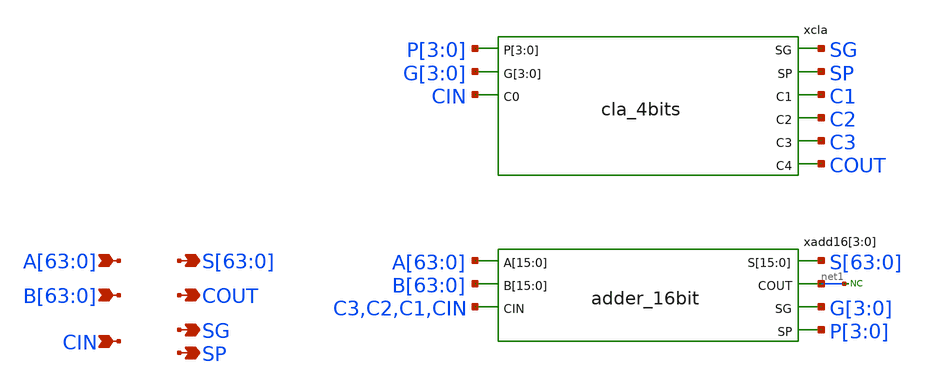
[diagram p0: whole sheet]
** sch_path: sky130A/xschem_libs/sky130_tests/adder_64bit/schematic/adder_64bit.sch
**.subckt adder_64bit
*+ A[63],A[62],A[61],A[60],A[59],A[58],A[57],A[56],A[55],A[54],A[53],A[52],A[51],A[50],A[49],A[48],A[47],A[46],A[45],A[44],A[43],A[42],A[41],A[40],A[39],A[38],A[37],A[36],A[35],A[34],A[33],A[32],A[31],A[30],A[29],A[28],A[27],A[26],A[25],A[24],A[23],A[22],A[21],A[20],A[19],A[18],A[17],A[16],A[15],A[14],A[13],A[12],A[11],A[10],A[9],A[8],A[7],A[6],A[5],A[4],A[3],A[2],A[1],A[0]
*+ B[63],B[62],B[61],B[60],B[59],B[58],B[57],B[56],B[55],B[54],B[53],B[52],B[51],B[50],B[49],B[48],B[47],B[46],B[45],B[44],B[43],B[42],B[41],B[40],B[39],B[38],B[37],B[36],B[35],B[34],B[33],B[32],B[31],B[30],B[29],B[28],B[27],B[26],B[25],B[24],B[23],B[22],B[21],B[20],B[19],B[18],B[17],B[16],B[15],B[14],B[13],B[12],B[11],B[10],B[9],B[8],B[7],B[6],B[5],B[4],B[3],B[2],B[1],B[0] CIN
*+ S[63],S[62],S[61],S[60],S[59],S[58],S[57],S[56],S[55],S[54],S[53],S[52],S[51],S[50],S[49],S[48],S[47],S[46],S[45],S[44],S[43],S[42],S[41],S[40],S[39],S[38],S[37],S[36],S[35],S[34],S[33],S[32],S[31],S[30],S[29],S[28],S[27],S[26],S[25],S[24],S[23],S[22],S[21],S[20],S[19],S[18],S[17],S[16],S[15],S[14],S[13],S[12],S[11],S[10],S[9],S[8],S[7],S[6],S[5],S[4],S[3],S[2],S[1],S[0] SP SG COUT
*.ipin
*+ A[63],A[62],A[61],A[60],A[59],A[58],A[57],A[56],A[55],A[54],A[53],A[52],A[51],A[50],A[49],A[48],A[47],A[46],A[45],A[44],A[43],A[42],A[41],A[40],A[39],A[38],A[37],A[36],A[35],A[34],A[33],A[32],A[31],A[30],A[29],A[28],A[27],A[26],A[25],A[24],A[23],A[22],A[21],A[20],A[19],A[18],A[17],A[16],A[15],A[14],A[13],A[12],A[11],A[10],A[9],A[8],A[7],A[6],A[5],A[4],A[3],A[2],A[1],A[0]
*.ipin
*+ B[63],B[62],B[61],B[60],B[59],B[58],B[57],B[56],B[55],B[54],B[53],B[52],B[51],B[50],B[49],B[48],B[47],B[46],B[45],B[44],B[43],B[42],B[41],B[40],B[39],B[38],B[37],B[36],B[35],B[34],B[33],B[32],B[31],B[30],B[29],B[28],B[27],B[26],B[25],B[24],B[23],B[22],B[21],B[20],B[19],B[18],B[17],B[16],B[15],B[14],B[13],B[12],B[11],B[10],B[9],B[8],B[7],B[6],B[5],B[4],B[3],B[2],B[1],B[0]
*.ipin CIN
*.opin
*+ S[63],S[62],S[61],S[60],S[59],S[58],S[57],S[56],S[55],S[54],S[53],S[52],S[51],S[50],S[49],S[48],S[47],S[46],S[45],S[44],S[43],S[42],S[41],S[40],S[39],S[38],S[37],S[36],S[35],S[34],S[33],S[32],S[31],S[30],S[29],S[28],S[27],S[26],S[25],S[24],S[23],S[22],S[21],S[20],S[19],S[18],S[17],S[16],S[15],S[14],S[13],S[12],S[11],S[10],S[9],S[8],S[7],S[6],S[5],S[4],S[3],S[2],S[1],S[0]
*.opin SP
*.opin SG
*.opin COUT
xadd16[3] A[63] A[62] A[61] A[60] A[59] A[58] A[57] A[56] A[55] A[54] A[53] A[52] A[51] A[50] A[49]
+ A[48] S[63] S[62] S[61] S[60] S[59] S[58] S[57] S[56] S[55] S[54] S[53] S[52] S[51] S[50] S[49] S[48]
+ B[63] B[62] B[61] B[60] B[59] B[58] B[57] B[56] B[55] B[54] B[53] B[52] B[51] B[50] B[49] B[48] net1 G[3]
+ C3 P[3] adder_16bit
xadd16[2] A[47] A[46] A[45] A[44] A[43] A[42] A[41] A[40] A[39] A[38] A[37] A[36] A[35] A[34] A[33]
+ A[32] S[47] S[46] S[45] S[44] S[43] S[42] S[41] S[40] S[39] S[38] S[37] S[36] S[35] S[34] S[33] S[32]
+ B[47] B[46] B[45] B[44] B[43] B[42] B[41] B[40] B[39] B[38] B[37] B[36] B[35] B[34] B[33] B[32] net1 G[2]
+ C2 P[2] adder_16bit
xadd16[1] A[31] A[30] A[29] A[28] A[27] A[26] A[25] A[24] A[23] A[22] A[21] A[20] A[19] A[18] A[17]
+ A[16] S[31] S[30] S[29] S[28] S[27] S[26] S[25] S[24] S[23] S[22] S[21] S[20] S[19] S[18] S[17] S[16]
+ B[31] B[30] B[29] B[28] B[27] B[26] B[25] B[24] B[23] B[22] B[21] B[20] B[19] B[18] B[17] B[16] net1 G[1]
+ C1 P[1] adder_16bit
xadd16[0] A[15] A[14] A[13] A[12] A[11] A[10] A[9] A[8] A[7] A[6] A[5] A[4] A[3] A[2] A[1] A[0]
+ S[15] S[14] S[13] S[12] S[11] S[10] S[9] S[8] S[7] S[6] S[5] S[4] S[3] S[2] S[1] S[0] B[15] B[14] B[13]
+ B[12] B[11] B[10] B[9] B[8] B[7] B[6] B[5] B[4] B[3] B[2] B[1] B[0] net1 G[0] CIN P[0] adder_16bit
xcla SG SP C1 P[3] P[2] P[1] P[0] C2 G[3] G[2] G[1] G[0] C3 COUT CIN cla_4bits
* noconn #net1
**.ends

* expanding   symbol:  sky130_tests/adder_16bit.sym # of pins=7
** sym_path: sky130_tests/adder_16bit.sym
** sch_path: sky130_tests/adder_16bit.sch
.subckt adder_16bit A[15] A[14] A[13] A[12] A[11] A[10] A[9] A[8] A[7] A[6] A[5] A[4] A[3] A[2] A[1]
+ A[0] S[15] S[14] S[13] S[12] S[11] S[10] S[9] S[8] S[7] S[6] S[5] S[4] S[3] S[2] S[1] S[0] B[15] B[14]
+ B[13] B[12] B[11] B[10] B[9] B[8] B[7] B[6] B[5] B[4] B[3] B[2] B[1] B[0] COUT SG CIN SP
*.ipin A[15],A[14],A[13],A[12],A[11],A[10],A[9],A[8],A[7],A[6],A[5],A[4],A[3],A[2],A[1],A[0]
*.ipin B[15],B[14],B[13],B[12],B[11],B[10],B[9],B[8],B[7],B[6],B[5],B[4],B[3],B[2],B[1],B[0]
*.ipin CIN
*.opin S[15],S[14],S[13],S[12],S[11],S[10],S[9],S[8],S[7],S[6],S[5],S[4],S[3],S[2],S[1],S[0]
*.opin SP
*.opin SG
*.opin COUT
xadd4[3] A[15] A[14] A[13] A[12] S[15] S[14] S[13] S[12] B[15] B[14] B[13] B[12] net1 G[3] C3 P[3]
+ adder_4bit
xadd4[2] A[11] A[10] A[9] A[8] S[11] S[10] S[9] S[8] B[11] B[10] B[9] B[8] net1 G[2] C2 P[2]
+ adder_4bit
xadd4[1] A[7] A[6] A[5] A[4] S[7] S[6] S[5] S[4] B[7] B[6] B[5] B[4] net1 G[1] C1 P[1] adder_4bit
xadd4[0] A[3] A[2] A[1] A[0] S[3] S[2] S[1] S[0] B[3] B[2] B[1] B[0] net1 G[0] CIN P[0] adder_4bit
xcla SG SP C1 P[3] P[2] P[1] P[0] C2 G[3] G[2] G[1] G[0] C3 COUT CIN cla_4bits
* noconn #net1
.ends


* expanding   symbol:  sky130_tests/cla_4bits.sym # of pins=9
** sym_path: sky130_tests/cla_4bits.sym
** sch_path: sky130_tests/cla_4bits.sch
.subckt cla_4bits SG SP C1 P[3] P[2] P[1] P[0] C2 G[3] G[2] G[1] G[0] C3 C4 C0
*.ipin P[3],P[2],P[1],P[0]
*.ipin G[3],G[2],G[1],G[0]
*.ipin C0
*.opin C4
*.opin C3
*.opin C2
*.opin C1
*.opin SG
*.opin SP
x1 P[0] VSS VSS VCC VCC net4 sky130_fd_sc_hd__inv_1
x2 net5 VSS VSS VCC VCC C1 sky130_fd_sc_hd__inv_1
x3 P[1] VSS VSS VCC VCC net2 sky130_fd_sc_hd__inv_1
x4 net8 VSS VSS VCC VCC C3 sky130_fd_sc_hd__inv_1
x5 G[1] VSS VSS VCC VCC net3 sky130_fd_sc_hd__inv_1
x6 net12 VSS VSS VCC VCC net13 sky130_fd_sc_hd__inv_1
x7 G[1] P[2] G[2] VSS VSS VCC VCC net12 sky130_fd_sc_hd__a21oi_1
x8 P[3] net13 G[3] VSS VSS VCC VCC net14 sky130_fd_sc_hd__a21oi_1
x9 C0 P[0] G[0] VSS VSS VCC VCC net5 sky130_fd_sc_hd__a21oi_1
x10 P[2] C2 G[2] VSS VSS VCC VCC net8 sky130_fd_sc_hd__a21oi_1
x11 G[0] VSS VSS VCC VCC net1 sky130_fd_sc_hd__inv_1
x12 net2 net5 net3 VSS VSS VCC VCC C2 sky130_fd_sc_hd__o21ai_1
x13 net5 net10 net14 VSS VSS VCC VCC C4 sky130_fd_sc_hd__o21ai_1
x14 net1 net10 net14 VSS VSS VCC VCC SG sky130_fd_sc_hd__o21ai_1
x15 net4 net10 VSS VSS VCC VCC SP sky130_fd_sc_hd__nor2_1
x16 P[1] P[2] P[3] VSS VSS VCC VCC net10 sky130_fd_sc_hd__nand3_1
C2 net4 0 5f m=1
C1 net10 0 5f m=1
C3 net1 0 5f m=1
C4 net14 0 5f m=1
C5 net2 0 5f m=1
C6 net5 0 5f m=1
C7 net3 0 5f m=1
C8 net8 0 5f m=1
C9 net13 0 5f m=1
C10 net12 0 5f m=1
C19[3] P[3] 0 5f m=1
C19[2] P[2] 0 5f m=1
C19[1] P[1] 0 5f m=1
C19[0] P[0] 0 5f m=1
C18[3] G[3] 0 5f m=1
C18[2] G[2] 0 5f m=1
C18[1] G[1] 0 5f m=1
C18[0] G[0] 0 5f m=1
C17 C0 0 5f m=1
.ends


* expanding   symbol:  sky130_tests/adder_4bit.sym # of pins=7
** sym_path: sky130_tests/adder_4bit.sym
** sch_path: sky130_tests/adder_4bit.sch
.subckt adder_4bit A[3] A[2] A[1] A[0] S[3] S[2] S[1] S[0] B[3] B[2] B[1] B[0] COUT SG CIN SP
*.ipin A[3],A[2],A[1],A[0]
*.ipin B[3],B[2],B[1],B[0]
*.ipin CIN
*.opin S[3],S[2],S[1],S[0]
*.opin SP
*.opin SG
*.opin COUT
xcla SG SP C1 P[3] P[2] P[1] P[0] C2 G[3] G[2] G[1] G[0] C3 COUT CIN cla_4bits
xadd1[3] S[3] A[3] B[3] G[3] C3 P[3] adder_1bit
xadd1[2] S[2] A[2] B[2] G[2] C2 P[2] adder_1bit
xadd1[1] S[1] A[1] B[1] G[1] C1 P[1] adder_1bit
xadd1[0] S[0] A[0] B[0] G[0] CIN P[0] adder_1bit
.ends


* expanding   symbol:  sky130_tests/adder_1bit.sym # of pins=6
** sym_path: sky130_tests/adder_1bit.sym
** sch_path: sky130_tests/adder_1bit.sch
.subckt adder_1bit S A B G CIN P
*.ipin A
*.ipin B
*.ipin CIN
*.opin S
*.opin P
*.opin G
x4 A B VSS VSS VCC VCC G sky130_fd_sc_hd__and2_1
x2 A B VSS VSS VCC VCC P sky130_fd_sc_hd__xor2_1
x3 P CIN VSS VSS VCC VCC S sky130_fd_sc_hd__xor2_1
C1 G 0 5f m=1
C2 P 0 5f m=1
C3 S 0 5f m=1
.ends

.end
